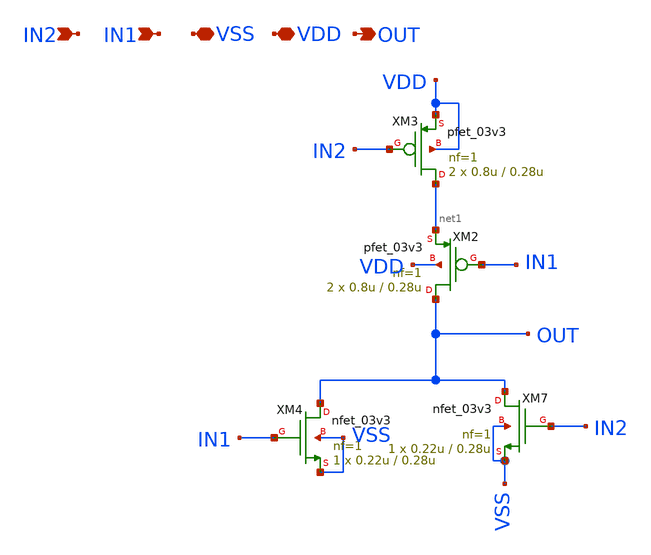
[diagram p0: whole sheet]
** sch_path: Clock_Generator_PAKISTAN_02/Schematics/nor_2.sch
**.subckt nor_2 IN2 IN1 VSS VDD OUT
*.ipin IN2
*.ipin IN1
*.iopin VSS
*.iopin VDD
*.opin OUT
XM4 OUT IN1 VSS VSS nfet_03v3 L=0.28u W=0.22u nf=1 ad='int((nf+1)/2) * W/nf * 0.18u' as='int((nf+2)/2) * W/nf * 0.18u'
+ pd='2*int((nf+1)/2) * (W/nf + 0.18u)' ps='2*int((nf+2)/2) * (W/nf + 0.18u)' nrd='0.18u / W' nrs='0.18u / W'
+ sa=0 sb=0 sd=0 m=1
XM2 OUT IN1 net1 VDD pfet_03v3 L=0.28u W=0.8u nf=1 ad='int((nf+1)/2) * W/nf * 0.18u' as='int((nf+2)/2) * W/nf * 0.18u'
+ pd='2*int((nf+1)/2) * (W/nf + 0.18u)' ps='2*int((nf+2)/2) * (W/nf + 0.18u)' nrd='0.18u / W' nrs='0.18u / W'
+ sa=0 sb=0 sd=0 m=2
XM7 OUT IN2 VSS VSS nfet_03v3 L=0.28u W=0.22u nf=1 ad='int((nf+1)/2) * W/nf * 0.18u' as='int((nf+2)/2) * W/nf * 0.18u'
+ pd='2*int((nf+1)/2) * (W/nf + 0.18u)' ps='2*int((nf+2)/2) * (W/nf + 0.18u)' nrd='0.18u / W' nrs='0.18u / W'
+ sa=0 sb=0 sd=0 m=1
XM3 net1 IN2 VDD VDD pfet_03v3 L=0.28u W=0.8u nf=1 ad='int((nf+1)/2) * W/nf * 0.18u' as='int((nf+2)/2) * W/nf * 0.18u'
+ pd='2*int((nf+1)/2) * (W/nf + 0.18u)' ps='2*int((nf+2)/2) * (W/nf + 0.18u)' nrd='0.18u / W' nrs='0.18u / W'
+ sa=0 sb=0 sd=0 m=2
**.ends
.end
